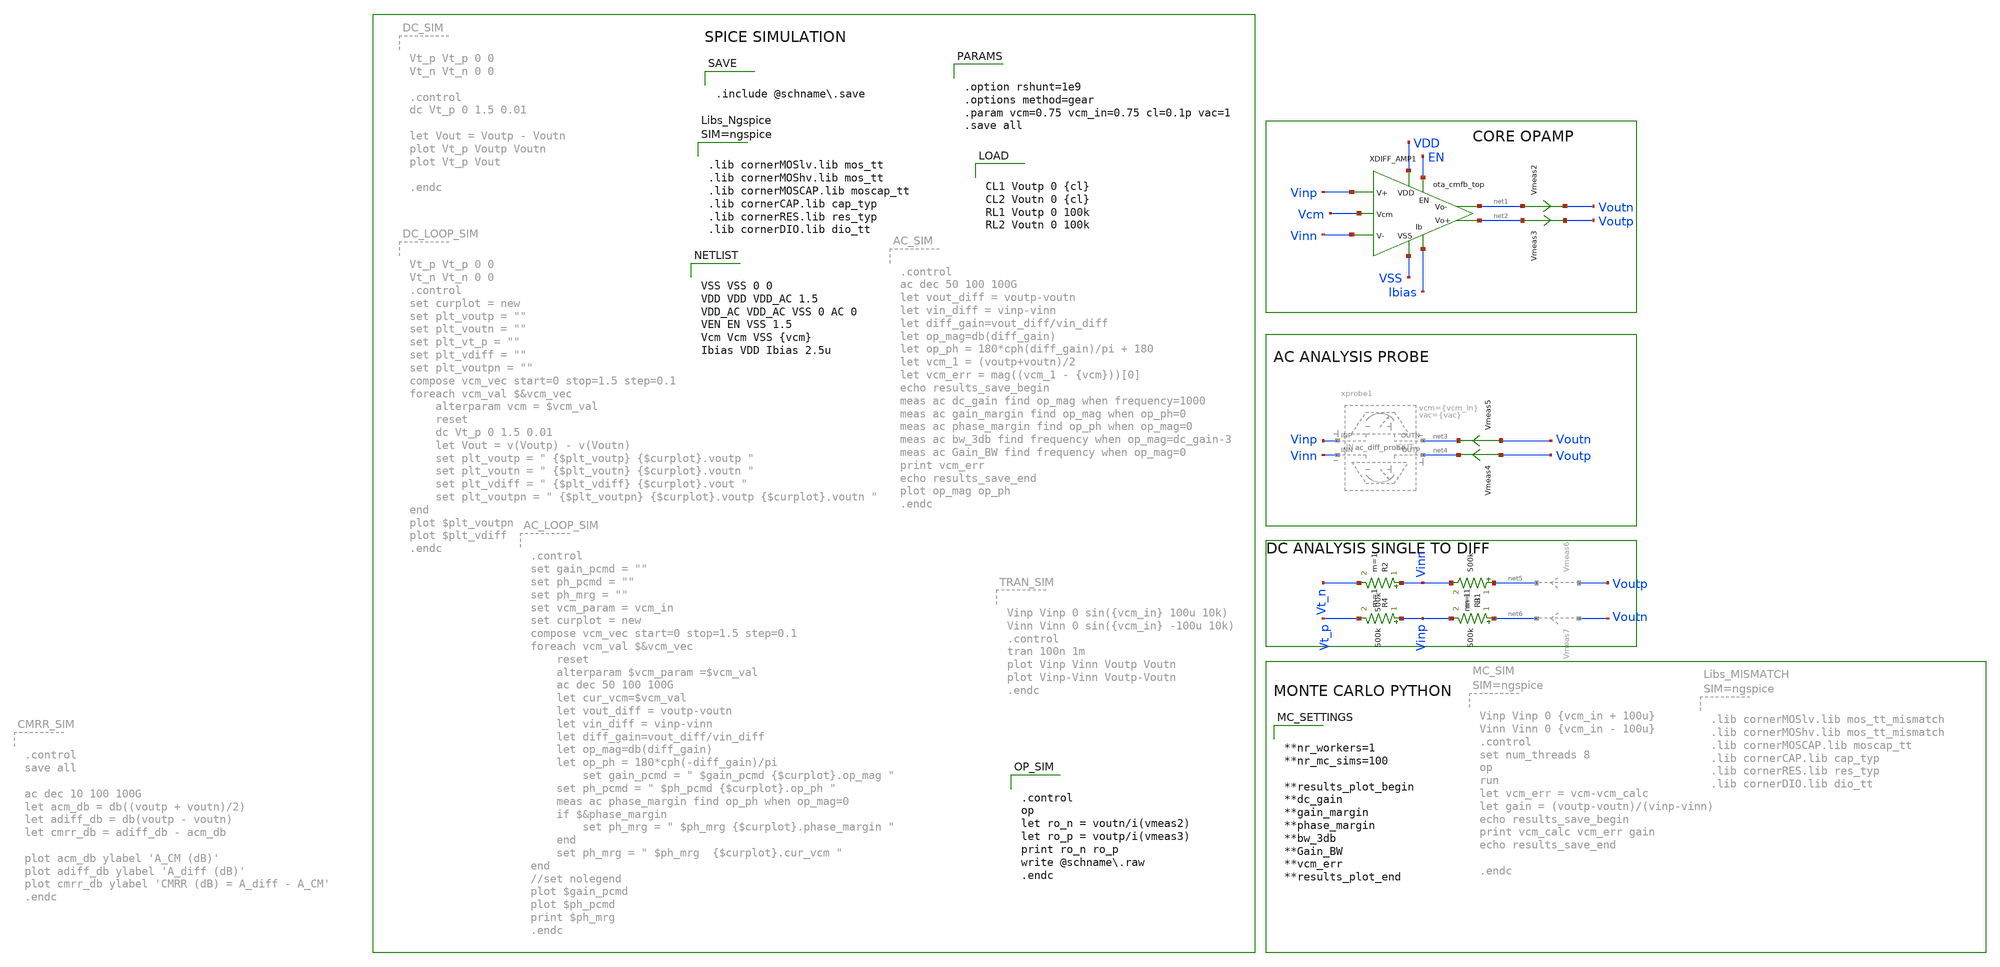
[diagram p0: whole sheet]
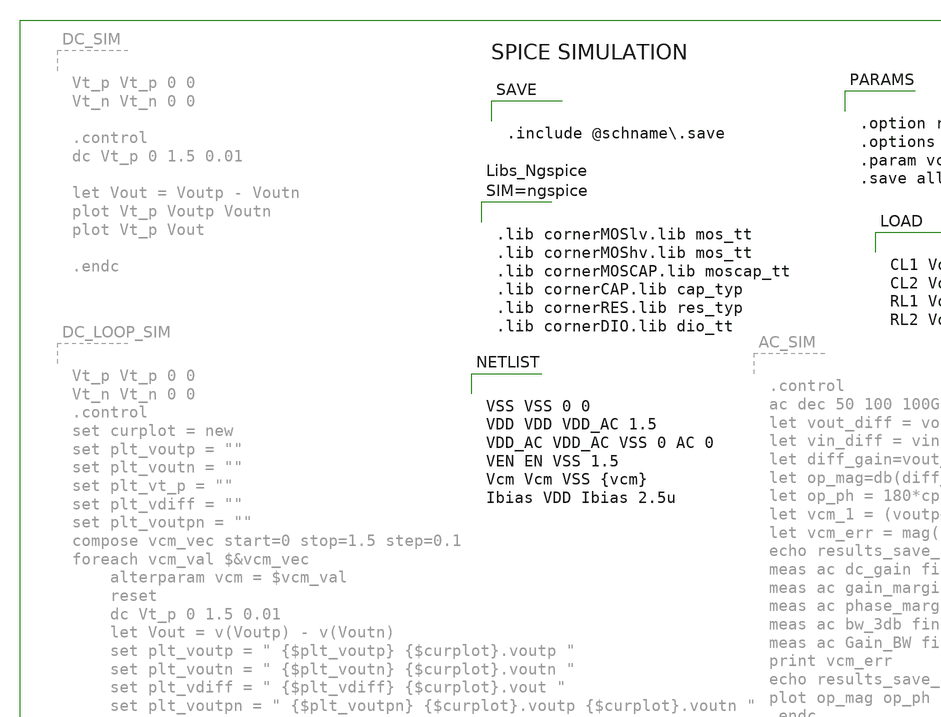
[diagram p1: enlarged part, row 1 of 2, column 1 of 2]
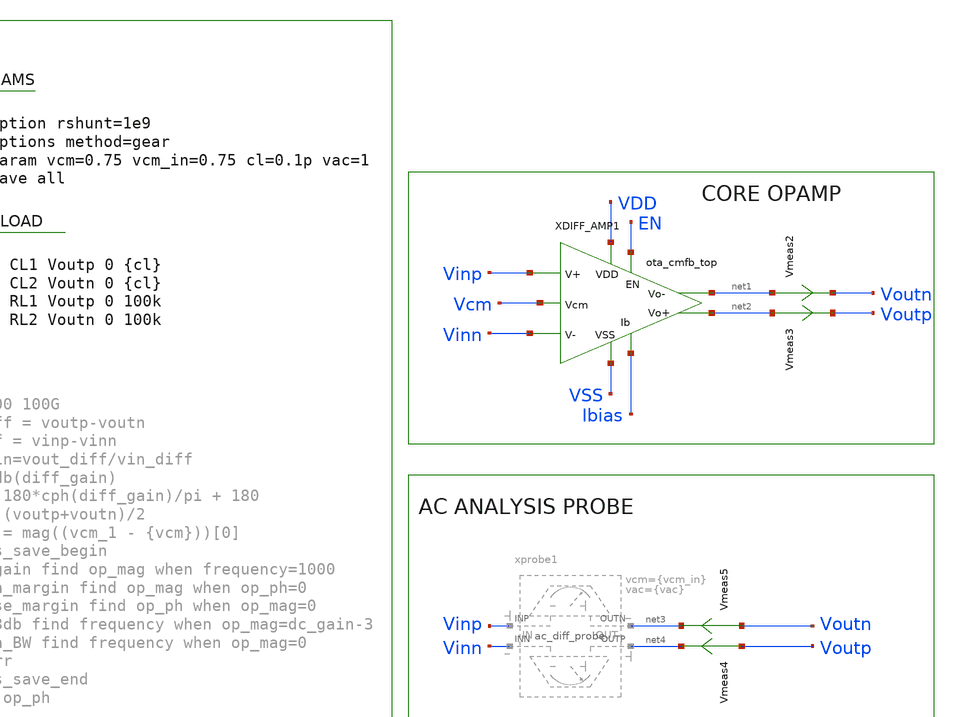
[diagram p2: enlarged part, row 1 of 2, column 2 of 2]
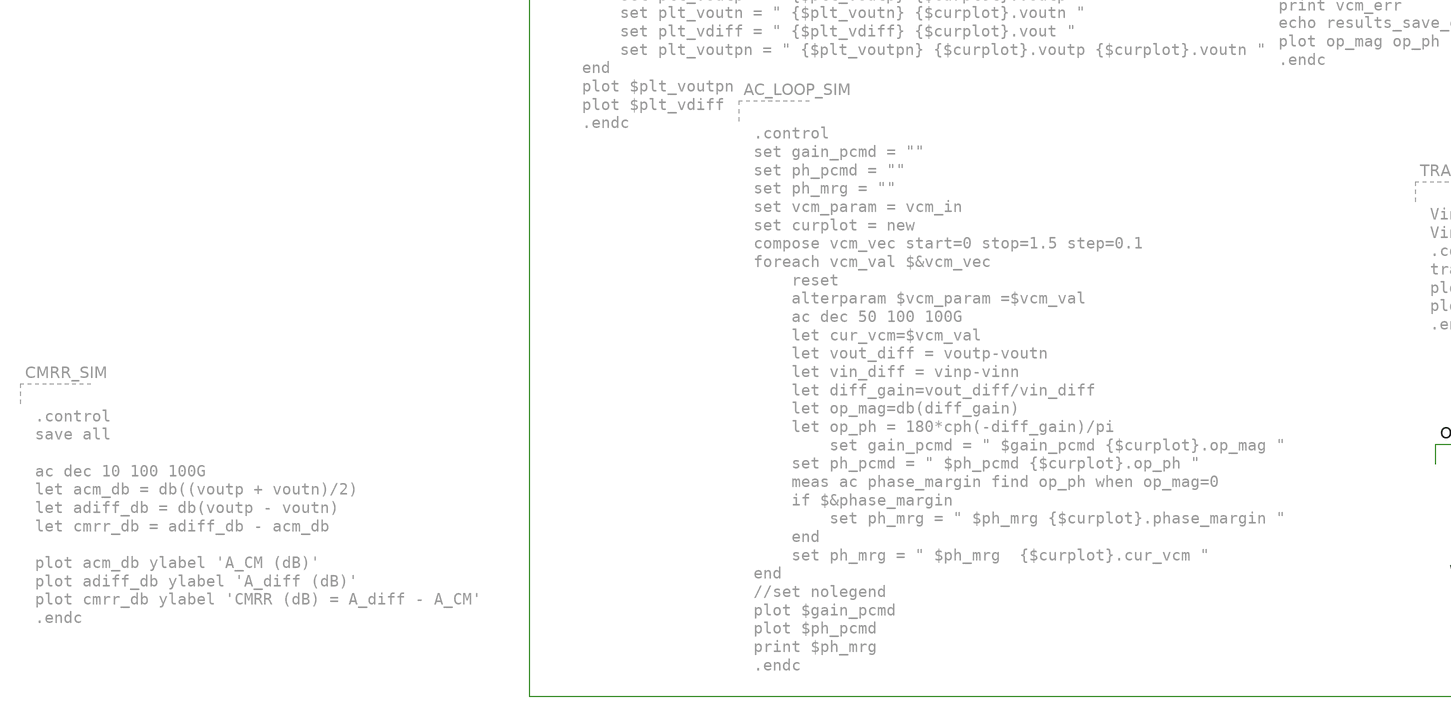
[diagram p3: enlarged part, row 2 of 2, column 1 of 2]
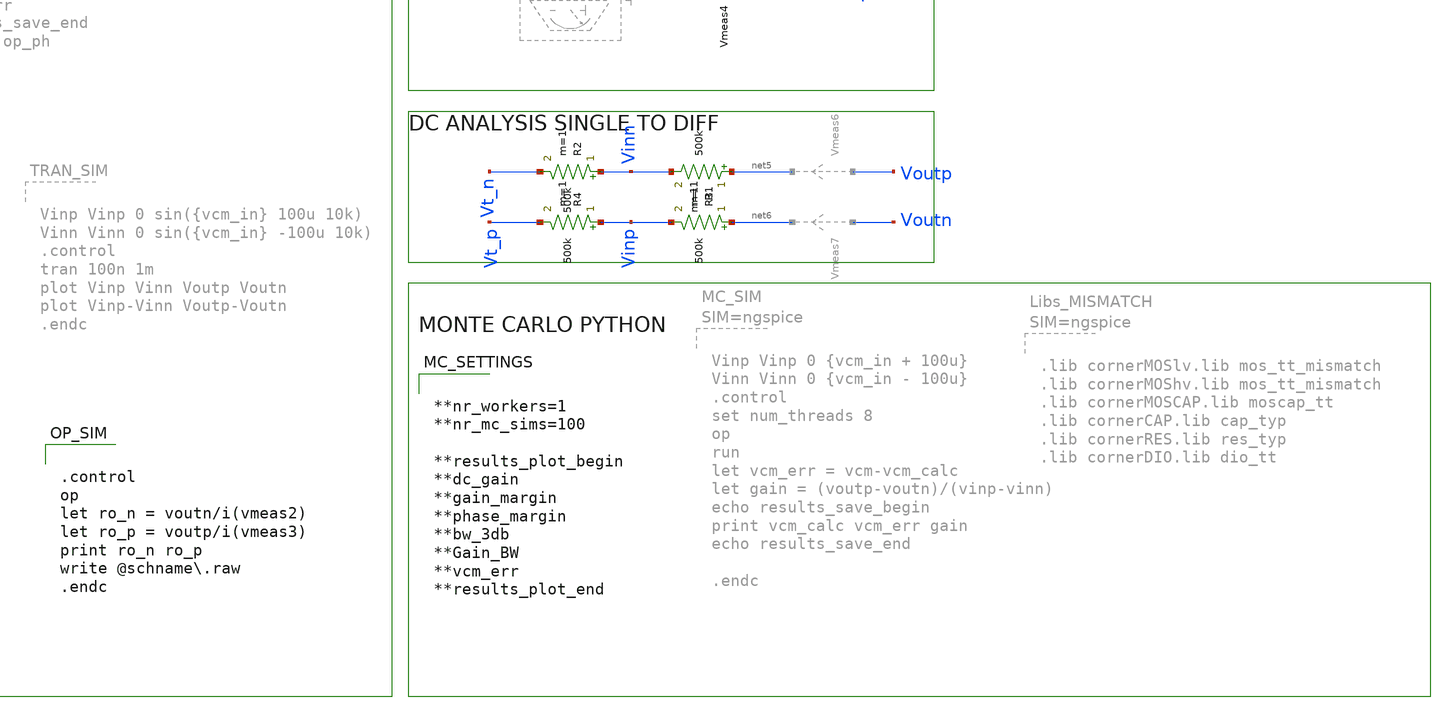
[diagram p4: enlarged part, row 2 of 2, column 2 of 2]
** sch_path: schema/ota_cmfb_top_tb.sch
**.subckt ota_cmfb_top_tb
Vmeas2 net1 Voutn 0
.save i(vmeas2)
Vmeas3 net2 Voutp 0
.save i(vmeas3)
Vmeas4 Voutp net4 0
.save i(vmeas4)
Vmeas5 Voutn net3 0
.save i(vmeas5)
R1 net5 Vinn 500k m=1
R2 Vinn Vt_n 500k m=1
R3 net6 Vinp 500k m=1
R4 Vinp Vt_p 500k m=1
XDIFF_AMP1 Vcm VDD EN Vinp net1 net2 Vinn VSS Ibias ota_cmfb_top
**** begin user architecture code


VSS VSS 0 0
VDD VDD VDD_AC 1.5
VDD_AC VDD_AC VSS 0 AC 0
VEN EN VSS 1.5
Vcm Vcm VSS {vcm}
Ibias VDD Ibias 2.5u



.control
op
let ro_n = voutn/i(vmeas2)
let ro_p = voutp/i(vmeas3)
print ro_n ro_p
write @schname.raw
.endc




.lib cornerMOSlv.lib mos_tt
.lib cornerMOShv.lib mos_tt
.lib cornerMOSCAP.lib moscap_tt
.lib cornerCAP.lib cap_typ
.lib cornerRES.lib res_typ
.lib cornerDIO.lib dio_tt





.option rshunt=1e9
.options method=gear
.param vcm=0.75 vcm_in=0.75 cl=0.1p vac=1
.save all




CL1 Voutp 0 {cl}
CL2 Voutn 0 {cl}
RL1 Voutp 0 100k
RL2 Voutn 0 100k



.include @schname.save



**nr_workers=1
**nr_mc_sims=100

**results_plot_begin
**dc_gain
**gain_margin
**phase_margin
**bw_3db
**Gain_BW
**vcm_err
**results_plot_end




VICM  vicm  0  DC 0.75
VDIFF vdiff 0  DC 0 AC 1
EIP Vinp vicm vdiff 0  0.5
EIN Vinn vicm vdiff 0 -0.5
EOD vod 0 Voutp Voutn 1

.control
save all
noise v(vod) VDIFF dec 10 1 10k
run
noise v(vod) VDIFF dec 10 1 10Meg
setplot noise3
plot loglog inoise_spectrum onoise_spectrum
setplot noise2
print inoise_total onoise_total
.endc


**** end user architecture code
**.ends
.end
